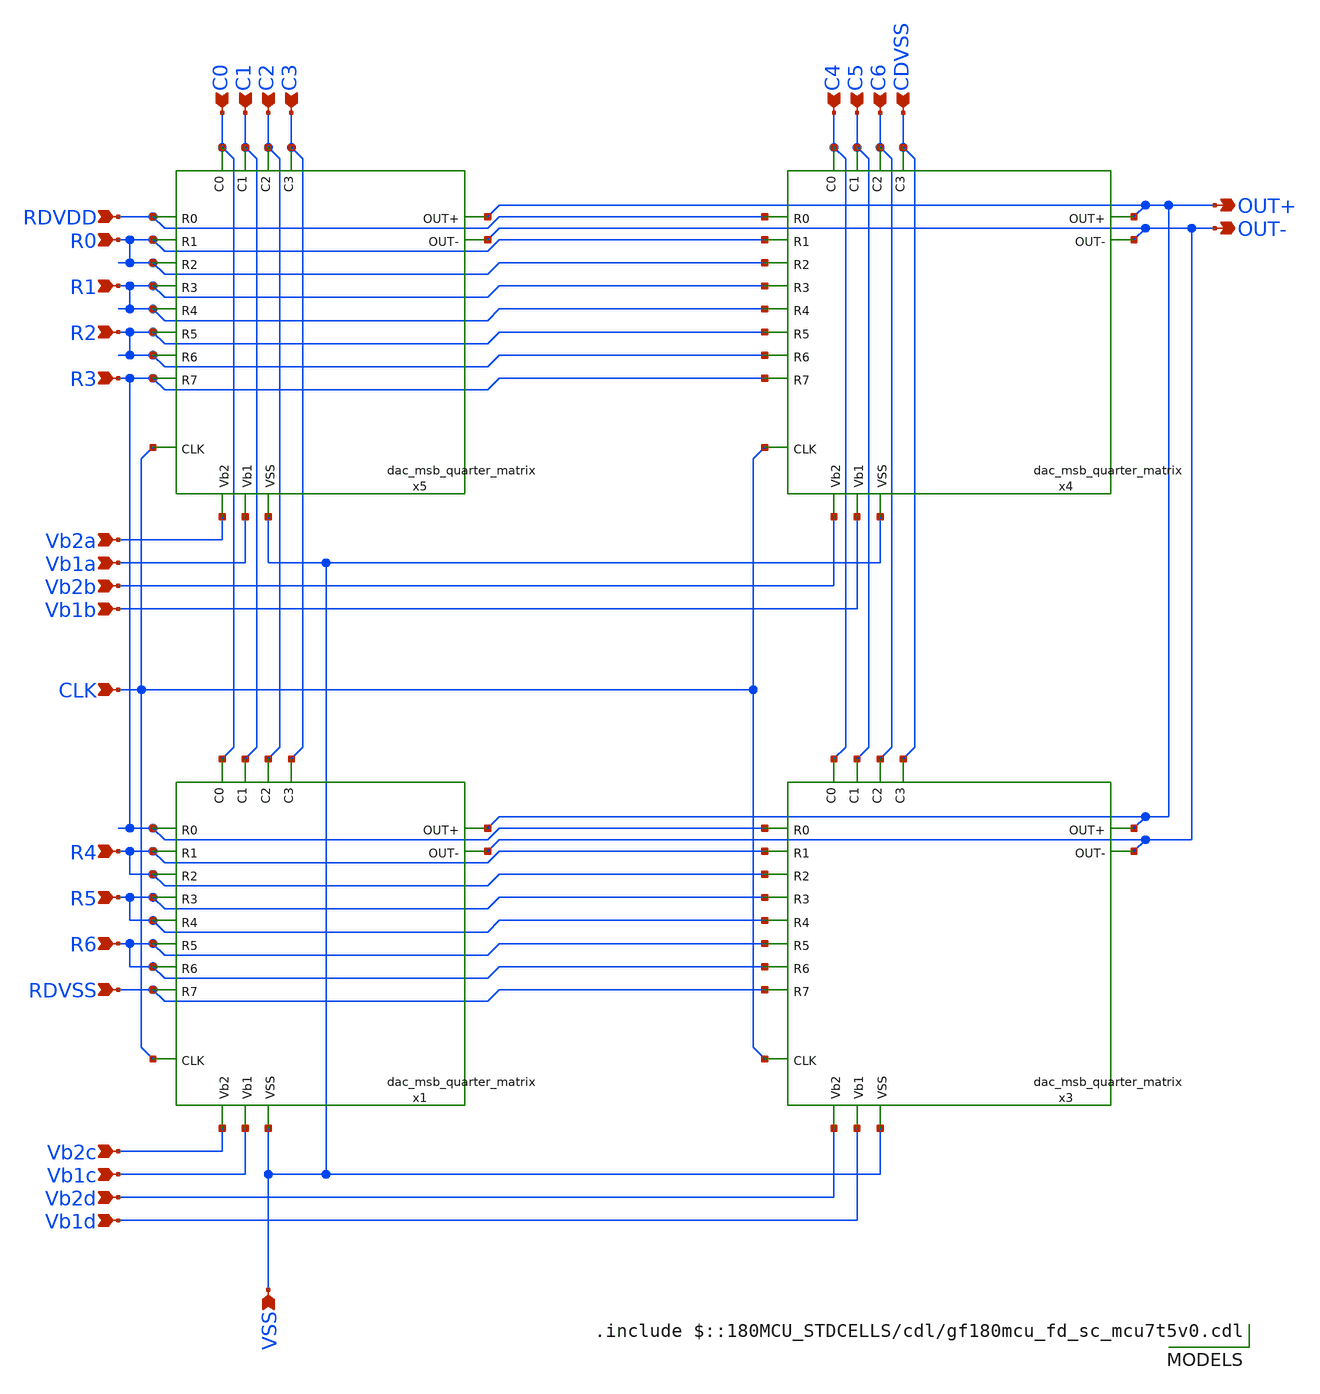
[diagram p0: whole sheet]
** sch_path: DAC/xschem/dac_msb_matrix.sch
**.subckt dac_msb_matrix R0 R1 R2 R3 R4 R5 R6 C0 C1 C2 C3 C4 C5 C6 VSS Vb2a Vb1a Vb2b Vb1b Vb2c Vb1c
*+ Vb2d Vb1d OUT+ OUT- CLK RDVDD RDVSS CDVSS
*.ipin R0
*.ipin R1
*.ipin R2
*.ipin R3
*.ipin R4
*.ipin R5
*.ipin R6
*.ipin C0
*.ipin C1
*.ipin C2
*.ipin C3
*.ipin C4
*.ipin C5
*.ipin C6
*.ipin VSS
*.ipin Vb2a
*.ipin Vb1a
*.ipin Vb2b
*.ipin Vb1b
*.ipin Vb2c
*.ipin Vb1c
*.ipin Vb2d
*.ipin Vb1d
*.opin OUT+
*.opin OUT-
*.ipin CLK
*.ipin RDVDD
*.ipin RDVSS
*.ipin CDVSS
x1 R3 R4 R4 R5 R5 R6 R6 RDVSS C0 C1 C2 C3 CLK Vb2c Vb1c VSS OUT+ OUT- DVDD DVSS
+ dac_msb_quarter_matrix
x3 R3 R4 R4 R5 R5 R6 R6 RDVSS C4 C5 C6 CDVSS CLK Vb2d Vb1d VSS OUT+ OUT- DVDD DVSS
+ dac_msb_quarter_matrix
x4 RDVDD R0 R0 R1 R1 R2 R2 R3 C4 C5 C6 CDVSS CLK Vb2b Vb1b VSS OUT+ OUT- DVDD DVSS
+ dac_msb_quarter_matrix
x5 RDVDD R0 R0 R1 R1 R2 R2 R3 C0 C1 C2 C3 CLK Vb2a Vb1a VSS OUT+ OUT- DVDD DVSS
+ dac_msb_quarter_matrix
**** begin user architecture code

.include $::180MCU_STDCELLS/cdl/gf180mcu_fd_sc_mcu7t5v0.cdl

**** end user architecture code
**.ends

* expanding   symbol:  dac_msb_quarter_matrix.sym # of pins=18
** sym_path: DAC/xschem/dac_msb_quarter_matrix.sym
** sch_path: DAC/xschem/dac_msb_quarter_matrix.sch
.subckt dac_msb_quarter_matrix R0 R1 R2 R3 R4 R5 R6 R7 C0 C1 C2 C3 CLK Vb2 Vb1 VSS OUT+ OUT- DVDD
+ DVSS
*.ipin CLK
*.ipin R0
*.ipin R1
*.ipin R2
*.ipin R3
*.ipin R4
*.ipin R5
*.ipin R6
*.ipin R7
*.ipin C0
*.ipin C1
*.ipin C2
*.ipin C3
*.ipin VSS
*.ipin Vb2
*.ipin Vb1
*.opin OUT+
*.opin OUT-
x13 C0 R6 R7 CLK Vb2 Vb1 VSS OUT+ OUT- DVDD DVSS dac_msb_cell
x1 C1 R6 R7 CLK Vb2 Vb1 VSS OUT+ OUT- DVDD DVSS dac_msb_cell
x3 C2 R6 R7 CLK Vb2 Vb1 VSS OUT+ OUT- DVDD DVSS dac_msb_cell
x5 C3 R6 R7 CLK Vb2 Vb1 VSS OUT+ OUT- DVDD DVSS dac_msb_cell
x2 C0 R4 R5 CLK Vb2 Vb1 VSS OUT+ OUT- DVDD DVSS dac_msb_cell
x4 C1 R4 R5 CLK Vb2 Vb1 VSS OUT+ OUT- DVDD DVSS dac_msb_cell
x6 C2 R4 R5 CLK Vb2 Vb1 VSS OUT+ OUT- DVDD DVSS dac_msb_cell
x7 C3 R4 R5 CLK Vb2 Vb1 VSS OUT+ OUT- DVDD DVSS dac_msb_cell
x8 C0 R2 R3 CLK Vb2 Vb1 VSS OUT+ OUT- DVDD DVSS dac_msb_cell
x9 C1 R2 R3 CLK Vb2 Vb1 VSS OUT+ OUT- DVDD DVSS dac_msb_cell
x10 C2 R2 R3 CLK Vb2 Vb1 VSS OUT+ OUT- DVDD DVSS dac_msb_cell
x11 C3 R2 R3 CLK Vb2 Vb1 VSS OUT+ OUT- DVDD DVSS dac_msb_cell
x12 C0 R0 R1 CLK Vb2 Vb1 VSS OUT+ OUT- DVDD DVSS dac_msb_cell
x14 C1 R0 R1 CLK Vb2 Vb1 VSS OUT+ OUT- DVDD DVSS dac_msb_cell
x15 C2 R0 R1 CLK Vb2 Vb1 VSS OUT+ OUT- DVDD DVSS dac_msb_cell
x16 C3 R0 R1 CLK Vb2 Vb1 VSS OUT+ OUT- DVDD DVSS dac_msb_cell
.ends


* expanding   symbol:  dac_msb_cell.sym # of pins=9
** sym_path: DAC/xschem/dac_msb_cell.sym
** sch_path: DAC/xschem/dac_msb_cell.sch
.subckt dac_msb_cell Cj Ri Rk CLK Vb2 Vb1 VSS OUT+ OUT- DVDD DVSS
*.ipin Cj
*.ipin Rk
*.ipin Ri
*.ipin CLK
*.ipin Vb2
*.ipin Vb1
*.ipin VSS
*.opin OUT+
*.opin OUT-
x2 net4 CLK net1 DVDD DVDD DVSS DVSS gf180mcu_fd_sc_mcu7t5v0__dffq_1
x3 net1 net2 DVDD DVDD DVSS DVSS gf180mcu_fd_sc_mcu7t5v0__inv_1
x6 Cj Ri net3 DVDD DVDD DVSS DVSS gf180mcu_fd_sc_mcu7t5v0__and2_1
x4 net3 Rk net4 DVDD DVDD DVSS DVSS gf180mcu_fd_sc_mcu7t5v0__or2_1
x1 OUT+ OUT- net2 net1 Vb2 Vb1 VSS dac_msb_analog
.ends


* expanding   symbol:  dac_msb_analog.sym # of pins=7
** sym_path: DAC/xschem/dac_msb_analog.sym
** sch_path: DAC/xschem/dac_msb_analog.sch
.subckt dac_msb_analog OUT+ OUT- Q- Q+ Vb2 Vb1 VSS
*.ipin Q-
*.ipin Q+
*.ipin Vb1
*.ipin Vb2
*.opin OUT+
*.opin OUT-
*.ipin VSS
XM26 net1 Vb2 net2 VSS nfet_03v3 L=0.5u W=32u nf=16 ad='int((nf+1)/2) * W/nf * 0.18u' as='int((nf+2)/2) * W/nf * 0.18u'
+ pd='2*int((nf+1)/2) * (W/nf + 0.18u)' ps='2*int((nf+2)/2) * (W/nf + 0.18u)' nrd='0.18u / W' nrs='0.18u / W'
+ sa=0 sb=0 sd=0 m=1
XM27 net2 Vb1 VSS VSS nfet_03v3 L=0.5u W=32u nf=16 ad='int((nf+1)/2) * W/nf * 0.18u' as='int((nf+2)/2) * W/nf * 0.18u'
+ pd='2*int((nf+1)/2) * (W/nf + 0.18u)' ps='2*int((nf+2)/2) * (W/nf + 0.18u)' nrd='0.18u / W' nrs='0.18u / W'
+ sa=0 sb=0 sd=0 m=1
XM30 OUT+ Q+ net1 VSS nfet_03v3 L=0.5u W=16u nf=8 ad='int((nf+1)/2) * W/nf * 0.18u' as='int((nf+2)/2) * W/nf * 0.18u'
+ pd='2*int((nf+1)/2) * (W/nf + 0.18u)' ps='2*int((nf+2)/2) * (W/nf + 0.18u)' nrd='0.18u / W' nrs='0.18u / W'
+ sa=0 sb=0 sd=0 m=1
XM31 OUT- Q- net1 VSS nfet_03v3 L=0.5u W=16u nf=8 ad='int((nf+1)/2) * W/nf * 0.18u' as='int((nf+2)/2) * W/nf * 0.18u'
+ pd='2*int((nf+1)/2) * (W/nf + 0.18u)' ps='2*int((nf+2)/2) * (W/nf + 0.18u)' nrd='0.18u / W' nrs='0.18u / W'
+ sa=0 sb=0 sd=0 m=1
.ends

.end
